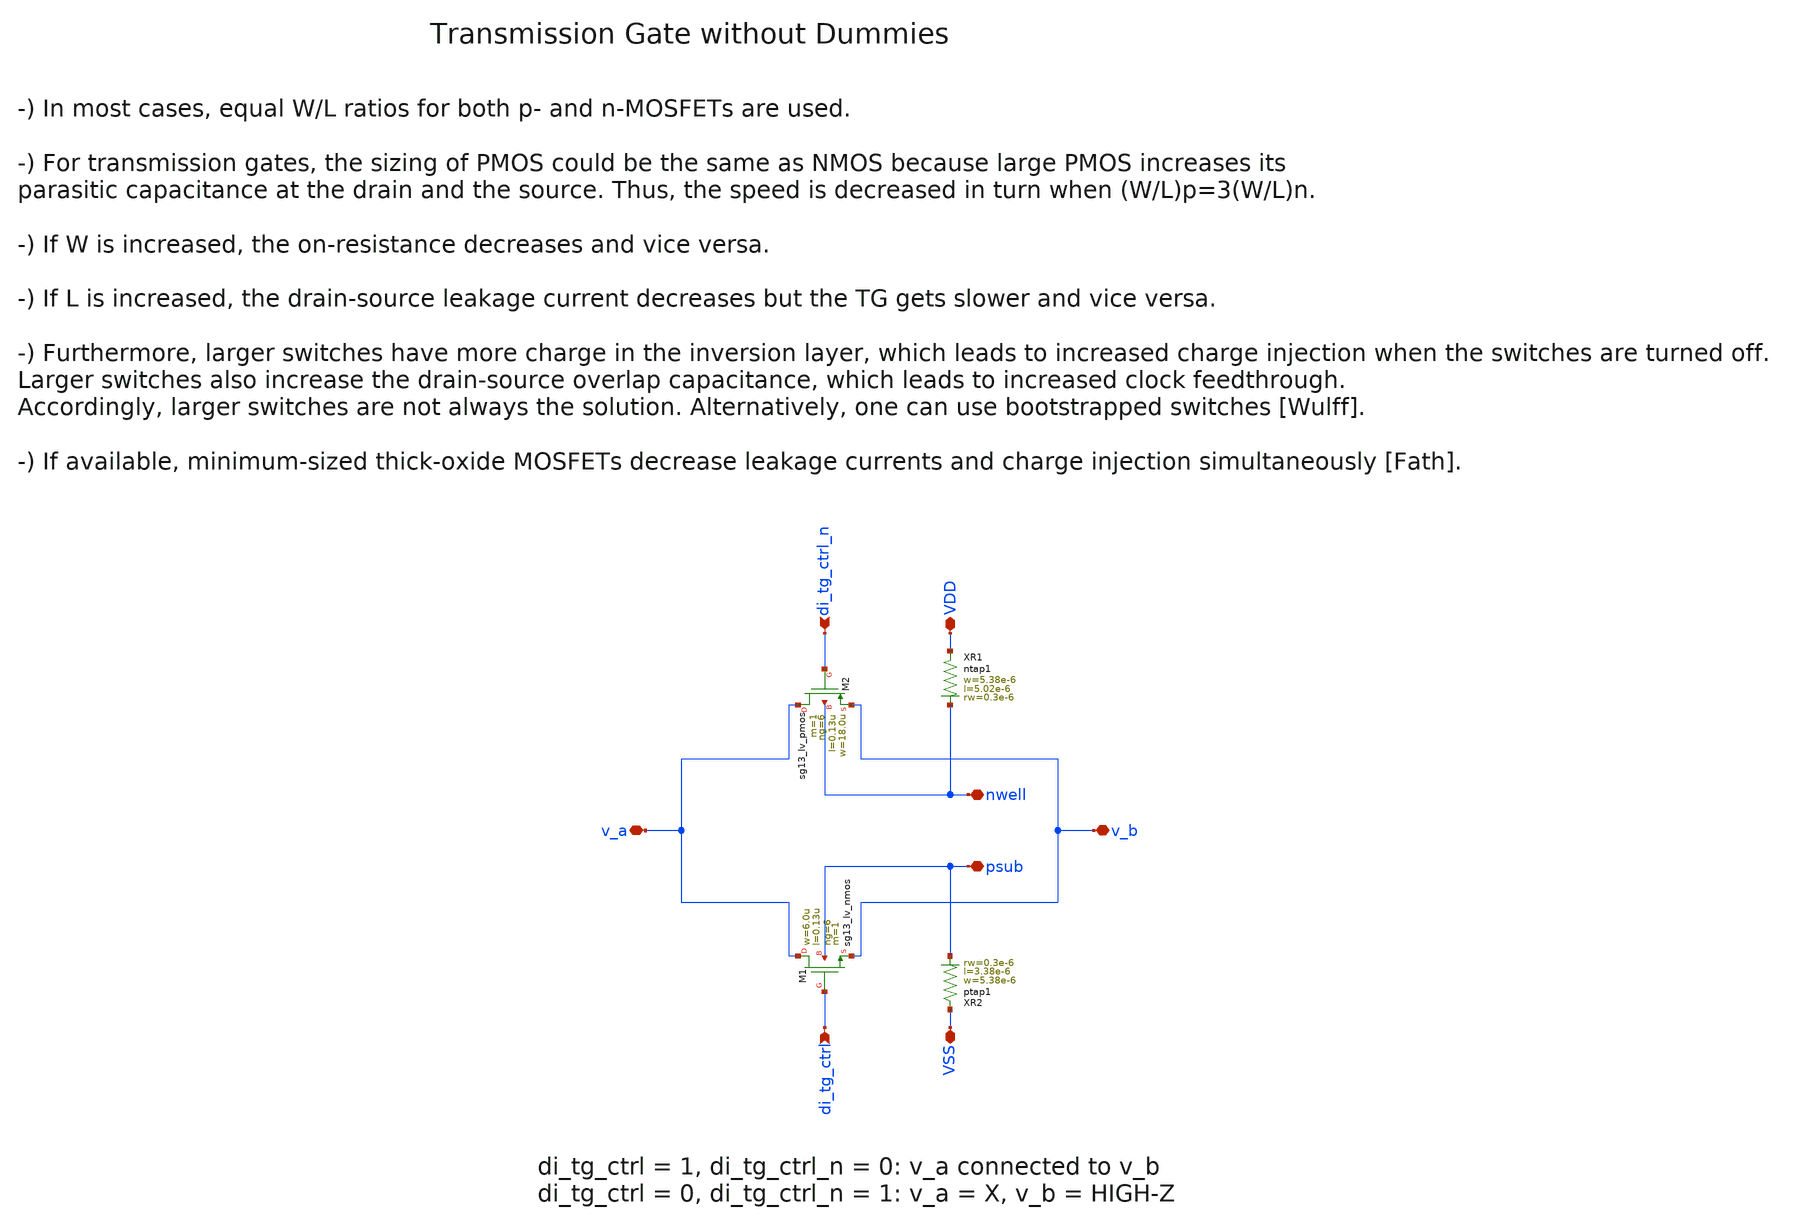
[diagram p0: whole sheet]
** sch_path: ihp130/macros/iqmod/schematic/iqmod_mixer_se2diff_tg_NF6.sch
**.subckt iqmod_mixer_se2diff_tg_NF6 v_a v_b VDD VSS di_tg_ctrl di_tg_ctrl_n nwell psub
*.iopin v_a
*.iopin v_b
*.iopin VDD
*.iopin VSS
*.ipin di_tg_ctrl
*.ipin di_tg_ctrl_n
*.iopin nwell
*.iopin psub
XM2 v_a di_tg_ctrl_n v_b nwell sg13_lv_pmos w=18.0u l=0.13u ng=6 m=1 mm_ok=1
XM1 v_a di_tg_ctrl v_b psub sg13_lv_nmos w=6.0u l=0.13u ng=6 m=1 mm_ok=1
XR1 VDD nwell ntap1 R=11.63 w=5.38e-6 l=5.02e-6 rw=0.3e-6
XR2 VSS psub ptap1 R=13.96 w=5.38e-6 l=3.38e-6 rw=0.3e-6
**.ends
.end
